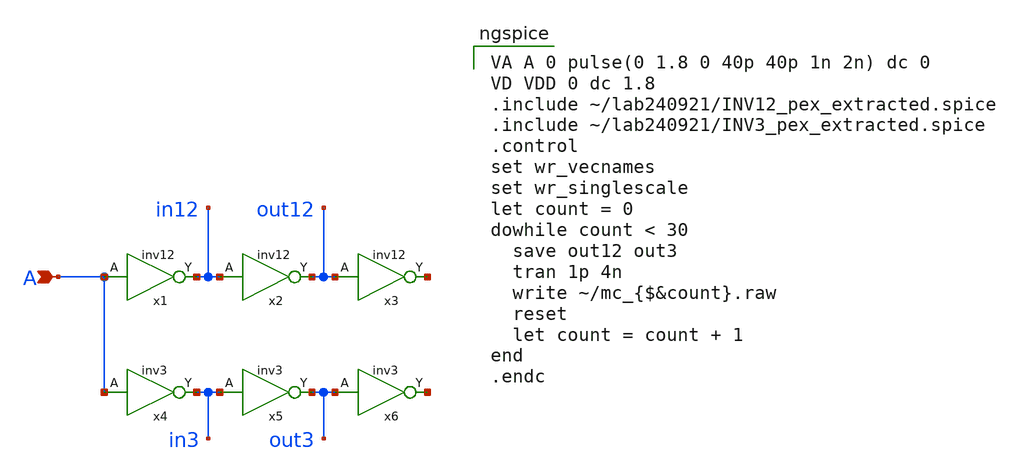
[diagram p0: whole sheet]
** sch_path: mm_sim.sch
**.subckt mm_sim A
*.ipin A
x1 A in12 VDD GND INV12
x2 in12 out12 VDD GND INV12
x3 out12 net1 VDD GND INV12
x4 A in3 VDD GND INV3
x5 in3 out3 VDD GND INV3
x6 out3 net2 VDD GND INV3
**** begin user architecture code

** opencircuitdesign pdks install
.lib $::SKYWATER_MODELS/sky130.lib.spice tt_mm



VA A 0 pulse(0 1.8 0 40p 40p 1n 2n) dc 0
VD VDD 0 dc 1.8
.include ~/lab240921/INV12_pex_extracted.spice
.include ~/lab240921/INV3_pex_extracted.spice
.control
set wr_vecnames
set wr_singlescale
let count = 0
dowhile count < 30
  save out12 out3
  tran 1p 4n
  write ~/mc_{$&count}.raw
  reset
  let count = count + 1
end
.endc

**** end user architecture code
**.ends
.end
